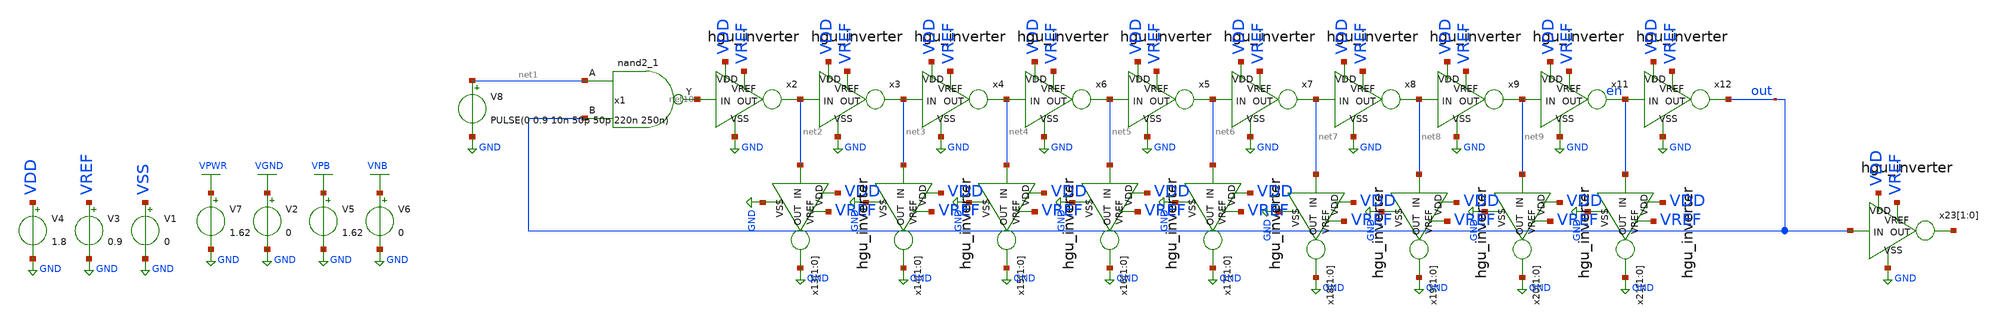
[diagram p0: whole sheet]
** sch_path: tb/untitled-1.sch
**.subckt untitled-1
V1 VSS GND 0
V3 VREF GND 0.9
V4 VDD GND 1.8
V8 net1 GND PULSE(0 0.9 10n 50p 50p 220n 250n)
x1 net1 out VGND VNB VPB VPWR net10 sky130_fd_sc_hd__nand2_1
x2 VDD net10 net2 GND VREF hgu_inverter
x3 VDD net2 net3 GND VREF hgu_inverter
x4 VDD net3 net4 GND VREF hgu_inverter
x6 VDD net4 net5 GND VREF hgu_inverter
x5 VDD net5 net6 GND VREF hgu_inverter
x7 VDD net6 net7 GND VREF hgu_inverter
x8 VDD net7 net8 GND VREF hgu_inverter
x9 VDD net8 net9 GND VREF hgu_inverter
x11 VDD net9 en GND VREF hgu_inverter
x12 VDD en out GND VREF hgu_inverter
x13[1] VDD net2 GND GND VREF hgu_inverter
x13[0] VDD net2 GND GND VREF hgu_inverter
x14[1] VDD net3 GND GND VREF hgu_inverter
x14[0] VDD net3 GND GND VREF hgu_inverter
x15[1] VDD net4 GND GND VREF hgu_inverter
x15[0] VDD net4 GND GND VREF hgu_inverter
x16[1] VDD net5 GND GND VREF hgu_inverter
x16[0] VDD net5 GND GND VREF hgu_inverter
x17[1] VDD net6 GND GND VREF hgu_inverter
x17[0] VDD net6 GND GND VREF hgu_inverter
x18[1] VDD net7 GND GND VREF hgu_inverter
x18[0] VDD net7 GND GND VREF hgu_inverter
x19[1] VDD net8 GND GND VREF hgu_inverter
x19[0] VDD net8 GND GND VREF hgu_inverter
x20[1] VDD net9 GND GND VREF hgu_inverter
x20[0] VDD net9 GND GND VREF hgu_inverter
x21[1] VDD en GND GND VREF hgu_inverter
x21[0] VDD en GND GND VREF hgu_inverter
x23[1] VDD out net11[1] GND VREF hgu_inverter
x23[0] VDD out net11[0] GND VREF hgu_inverter
V5 VPB GND 1.62
V6 VNB GND 0
V7 VPWR GND 1.62
V2 VGND GND 0
**** begin user architecture code



.OPTIONS savecurrents
.tran 10ps 200ns
.include /foss/designs/hgu_goss/hgu/mag/hgu_cdac_unit.spice
.lib /foss/pdks/sky130A/libs.tech/ngspice/sky130.lib.spice tt
.include /foss/pdks/sky130A/libs.ref/sky130_fd_sc_hd/spice/sky130_fd_sc_hd.spice

.control
	run
	let svdd = 0.9
	let max = svdd*0.8
	let min = svdd*0.2
	let mid = svdd*0.5
	meas tran rising_s1 find time when V(out)=min RISE=1 TD=1p
        meas tran rising_e1 find time when V(out)=max RISE=1 TD=1p
        let rising_time1 = rising_e1-rising_s1
        meas tran falling_s1 find time when V(out)=max FALL=1 TD=1p
        meas tran falling_e1 find time when V(out)=min FALL=1 TD=1p
        let falling_time1 = falling_e1-falling_s1


        print rising_time1 falling_time1
	plot v(en) v(out)
.endc
.save all



**** end user architecture code
**.ends
.GLOBAL GND
.GLOBAL VPB
.GLOBAL VNB
.GLOBAL VPWR
.GLOBAL VGND
.end
